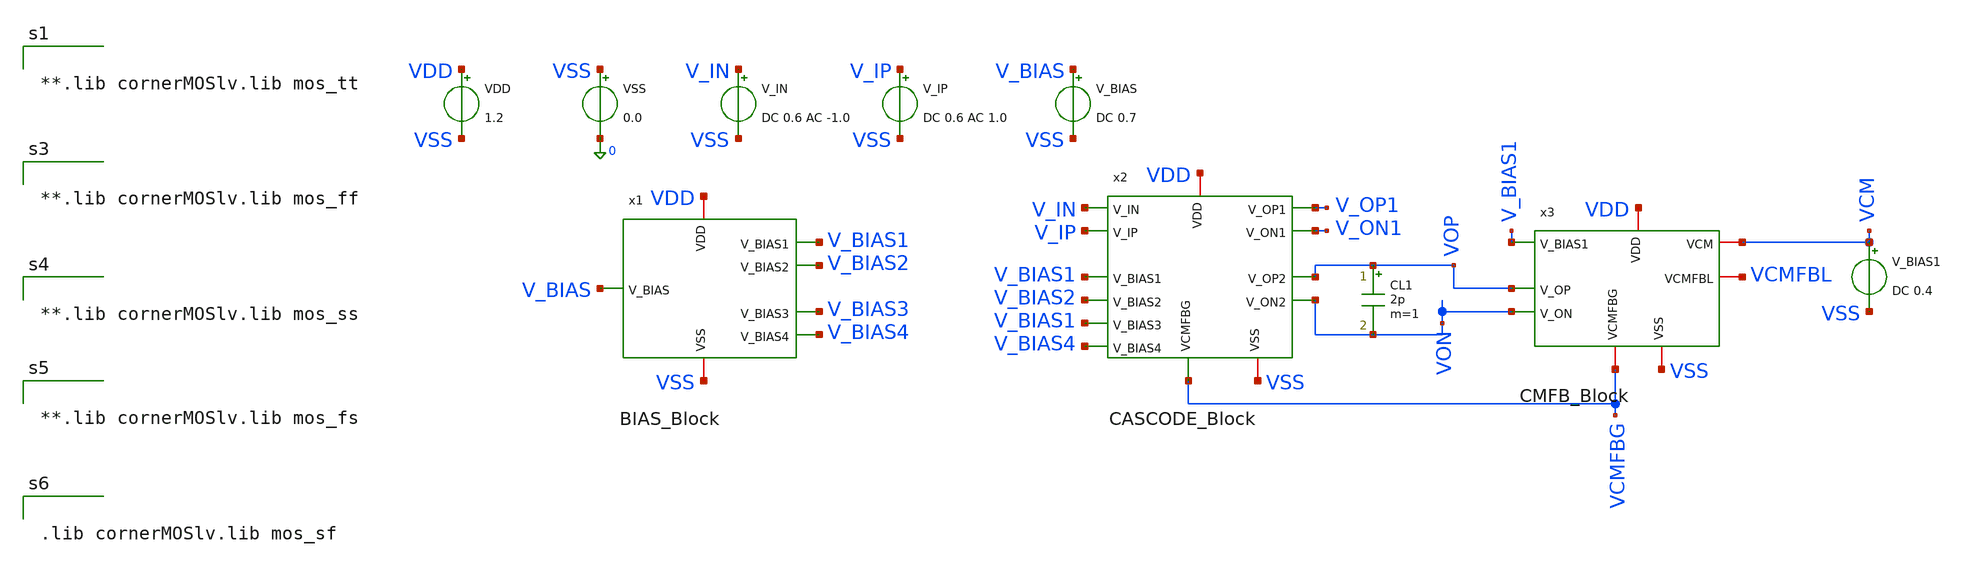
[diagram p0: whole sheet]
** sch_path: two-stage-ota-with-cmfb/Simulation/TEST_CORNER_PROCESS.sch
**.subckt TEST_CORNER_PROCESS
VDD VDD VSS 1.2
VSS VSS 0 0.0
V_IN V_IN VSS DC 0.6 AC -1.0
V_IP V_IP VSS DC 0.6 AC 1.0
V_BIAS V_BIAS VSS DC 0.7
V_BIAS1 VCM VSS DC 0.4
CL1 VOP VON 2p m=1
x1 VSS V_BIAS4 V_BIAS2 V_BIAS3 VDD V_BIAS1 V_BIAS BIAS_Block
x2 VDD V_BIAS1 V_IN V_IP V_BIAS2 V_ON1 V_OP1 V_BIAS1 VON VOP VCMFBG V_BIAS4 VSS CASCODE_Block
x3 VDD V_BIAS1 VCM VOP VON VCMFBL VCMFBG VSS CMFB_Block
**** begin user architecture code


.control
set color0=white
set color1=black

set temps = ( -40 27 85 )

foreach t $temps
  set temp = $t

  * 1. Phan tich AC
  ac dec 20 1 10G

  * Chuyen dung vao plot AC vua chay xong
  set acplot = $curplot
  setplot $acplot

  * Tinh do loi vi sai (dB)
  let a_diff = (v(vop) - v(von)) / (v(v_ip) - v(v_in))
  let gain_db = db(a_diff)

  * Doi pha tu Radian sang Do (Degree)
  let phase_deg = cph(a_diff) * 180 / pi

  meas ac dc_gain find gain_db at=1
  meas ac gbw when gain_db=0 fall=1
  meas ac phase_at_gbw find phase_deg when gain_db=0 fall=1
  let pm = 180 + phase_at_gbw

  * 2. Phan tich DC OP lay dong qua nguon VDD
  op
  set opplot = $curplot
  setplot $opplot
  let p_mw = abs(v(vdd) * vdd#branch) * 1e3

  * In ket qua day du
  echo '=================================================='
  echo 'KET QUA TAI NHIET DO:' $t 'DO C'
  echo '=================================================='
  setplot $acplot
  print dc_gain gbw pm
  setplot $opplot
  print p_mw
end
.endc




**.lib cornerMOSlv.lib mos_tt




**.lib cornerMOSlv.lib mos_ff




**.lib cornerMOSlv.lib mos_ss




**.lib cornerMOSlv.lib mos_fs




.lib cornerMOSlv.lib mos_sf


**** end user architecture code
**.ends
.end
